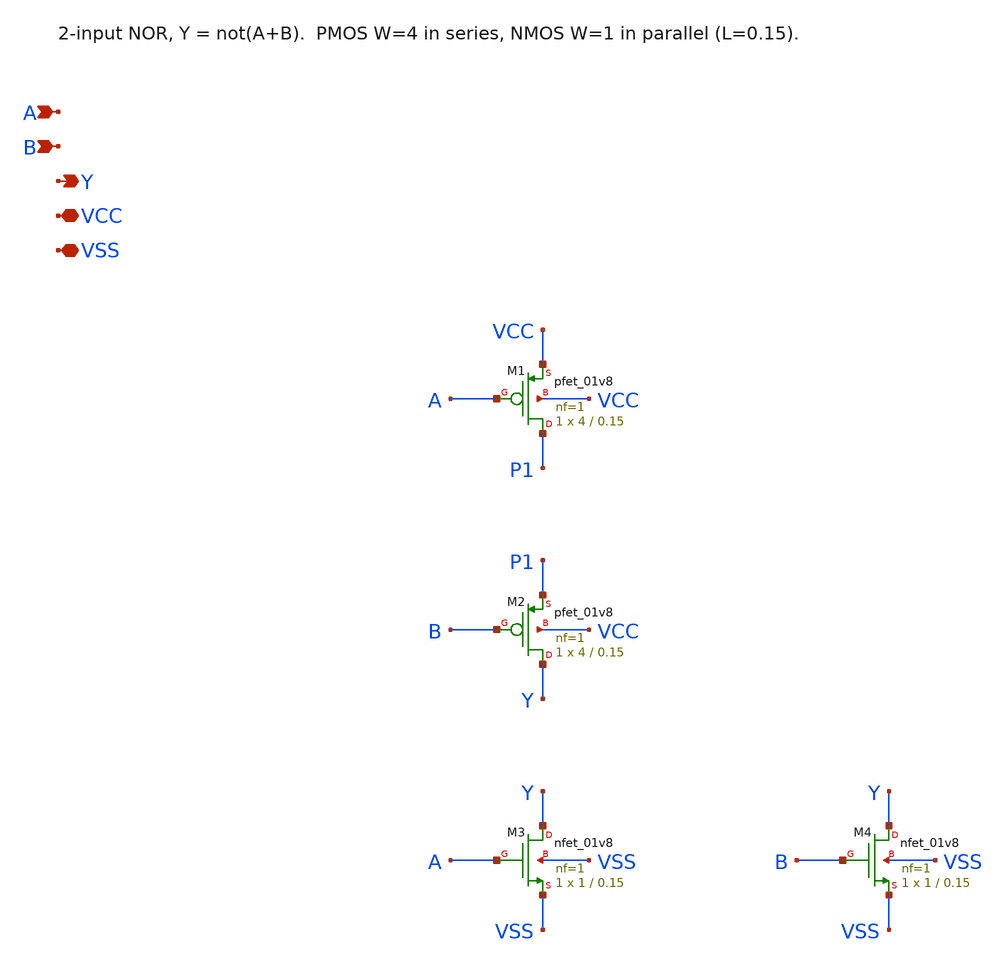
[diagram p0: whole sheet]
** sch_path: nor2.sch
**.subckt nor2 A B Y VCC VSS
*.ipin A
*.ipin B
*.opin Y
*.iopin VCC
*.iopin VSS
XM1 P1 A VCC VCC sky130_fd_pr__pfet_01v8 L=0.15 W=4 nf=1 ad='int((nf+1)/2) * W/nf * 0.29' as='int((nf+2)/2) * W/nf * 0.29'
+ pd='2*int((nf+1)/2) * (W/nf + 0.29)' ps='2*int((nf+2)/2) * (W/nf + 0.29)' nrd='0.29 / W' nrs='0.29 / W'
+ sa=0 sb=0 sd=0 mult=1 m=1
XM2 Y B P1 VCC sky130_fd_pr__pfet_01v8 L=0.15 W=4 nf=1 ad='int((nf+1)/2) * W/nf * 0.29' as='int((nf+2)/2) * W/nf * 0.29'
+ pd='2*int((nf+1)/2) * (W/nf + 0.29)' ps='2*int((nf+2)/2) * (W/nf + 0.29)' nrd='0.29 / W' nrs='0.29 / W'
+ sa=0 sb=0 sd=0 mult=1 m=1
XM3 Y A VSS VSS sky130_fd_pr__nfet_01v8 L=0.15 W=1 nf=1 ad='int((nf+1)/2) * W/nf * 0.29' as='int((nf+2)/2) * W/nf * 0.29'
+ pd='2*int((nf+1)/2) * (W/nf + 0.29)' ps='2*int((nf+2)/2) * (W/nf + 0.29)' nrd='0.29 / W' nrs='0.29 / W'
+ sa=0 sb=0 sd=0 mult=1 m=1
XM4 Y B VSS VSS sky130_fd_pr__nfet_01v8 L=0.15 W=1 nf=1 ad='int((nf+1)/2) * W/nf * 0.29' as='int((nf+2)/2) * W/nf * 0.29'
+ pd='2*int((nf+1)/2) * (W/nf + 0.29)' ps='2*int((nf+2)/2) * (W/nf + 0.29)' nrd='0.29 / W' nrs='0.29 / W'
+ sa=0 sb=0 sd=0 mult=1 m=1
**.ends
.end
